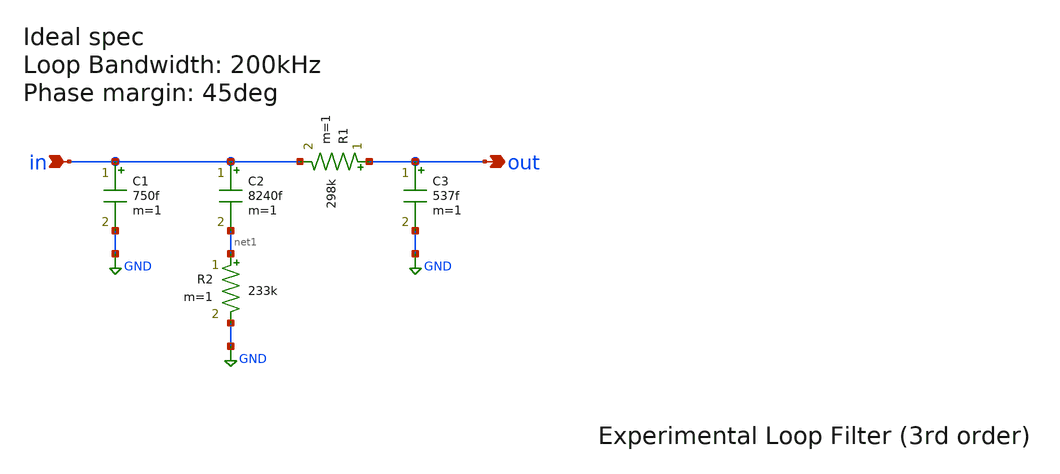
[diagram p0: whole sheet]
** sch_path: PLL/xschem/lf2.sch
**.subckt lf2 out in
*.opin out
*.ipin in
R2 net1 GND 233k m=1
C1 in GND 750f m=1
C2 in net1 8240f m=1
R1 out in 298k m=1
C3 out GND 537f m=1
**.ends
.GLOBAL GND
.end
